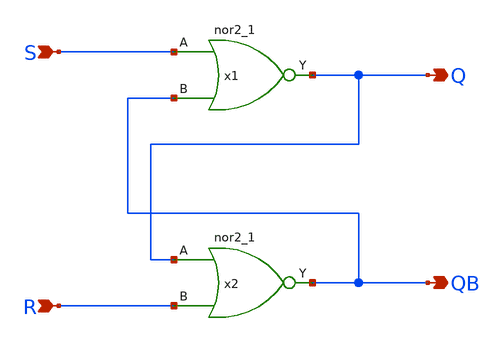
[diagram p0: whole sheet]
** sch_path: xschem/my_sr_latch.sch
**.subckt my_sr_latch S R Q QB
*.ipin S
*.ipin R
*.opin Q
*.opin QB
x1 S QB GND GND VDD VDD Q sky130_fd_sc_hd__nor2_1
x2 Q R GND GND VDD VDD QB sky130_fd_sc_hd__nor2_1
**.ends
.end
